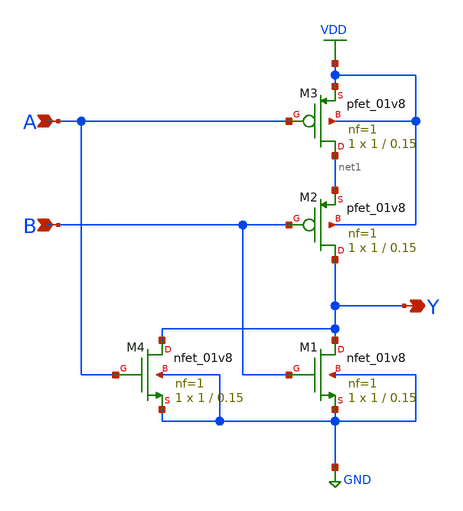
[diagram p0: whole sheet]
** sch_path: library/xschem/nor2.sch
**.subckt nor2 Y A B
*.opin Y
*.ipin A
*.ipin B
XM1 Y B GND GND sky130_fd_pr__nfet_01v8 L=0.15 W=1 nf=1 ad='int((nf+1)/2) * W/nf * 0.29' as='int((nf+2)/2) * W/nf * 0.29'
+ pd='2*int((nf+1)/2) * (W/nf + 0.29)' ps='2*int((nf+2)/2) * (W/nf + 0.29)' nrd='0.29 / W' nrs='0.29 / W'
+ sa=0 sb=0 sd=0 mult=1 m=1
XM2 Y B net1 VDD sky130_fd_pr__pfet_01v8 L=0.15 W=1 nf=1 ad='int((nf+1)/2) * W/nf * 0.29' as='int((nf+2)/2) * W/nf * 0.29'
+ pd='2*int((nf+1)/2) * (W/nf + 0.29)' ps='2*int((nf+2)/2) * (W/nf + 0.29)' nrd='0.29 / W' nrs='0.29 / W'
+ sa=0 sb=0 sd=0 mult=1 m=1
XM3 net1 A VDD VDD sky130_fd_pr__pfet_01v8 L=0.15 W=1 nf=1 ad='int((nf+1)/2) * W/nf * 0.29' as='int((nf+2)/2) * W/nf * 0.29'
+ pd='2*int((nf+1)/2) * (W/nf + 0.29)' ps='2*int((nf+2)/2) * (W/nf + 0.29)' nrd='0.29 / W' nrs='0.29 / W'
+ sa=0 sb=0 sd=0 mult=1 m=1
XM4 Y A GND GND sky130_fd_pr__nfet_01v8 L=0.15 W=1 nf=1 ad='int((nf+1)/2) * W/nf * 0.29' as='int((nf+2)/2) * W/nf * 0.29'
+ pd='2*int((nf+1)/2) * (W/nf + 0.29)' ps='2*int((nf+2)/2) * (W/nf + 0.29)' nrd='0.29 / W' nrs='0.29 / W'
+ sa=0 sb=0 sd=0 mult=1 m=1
**.ends
.GLOBAL VDD
.GLOBAL GND
.end
